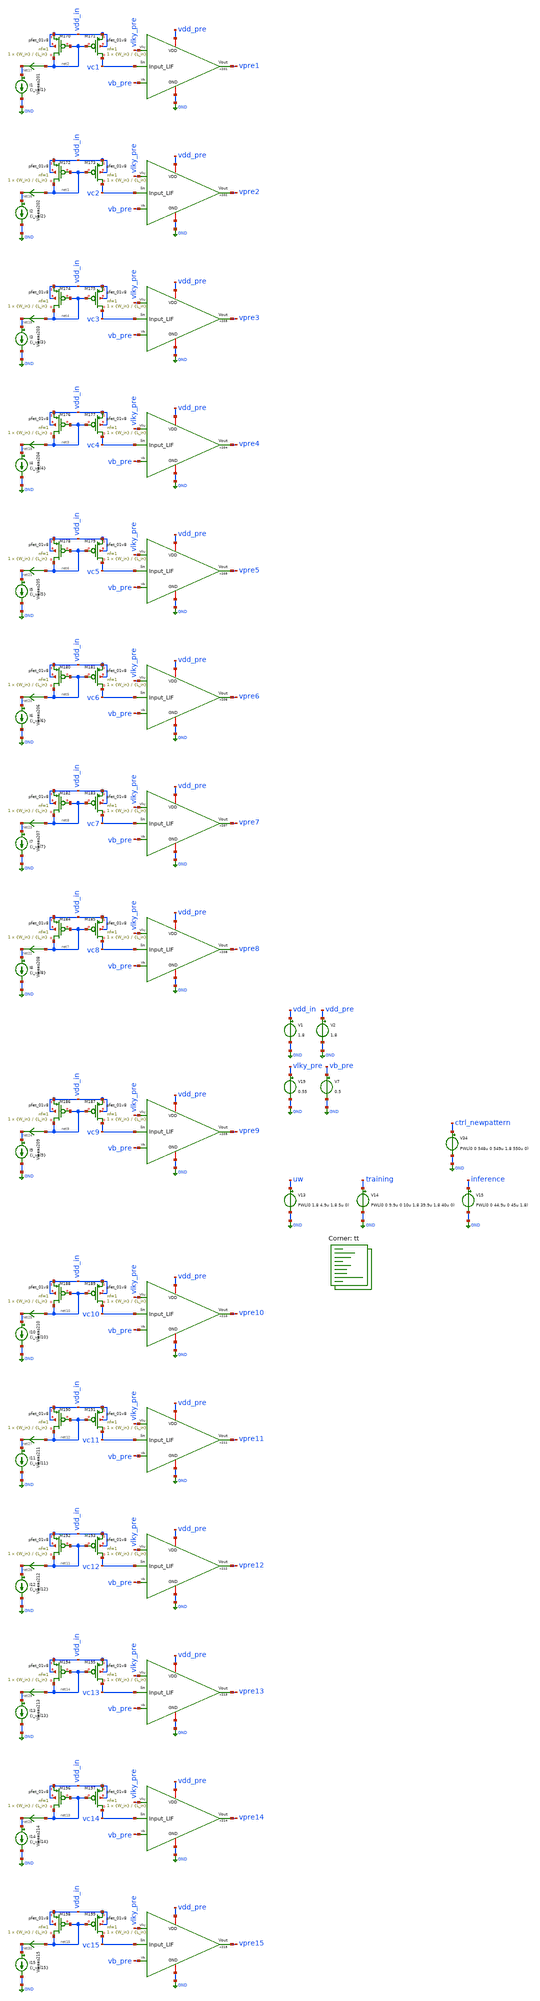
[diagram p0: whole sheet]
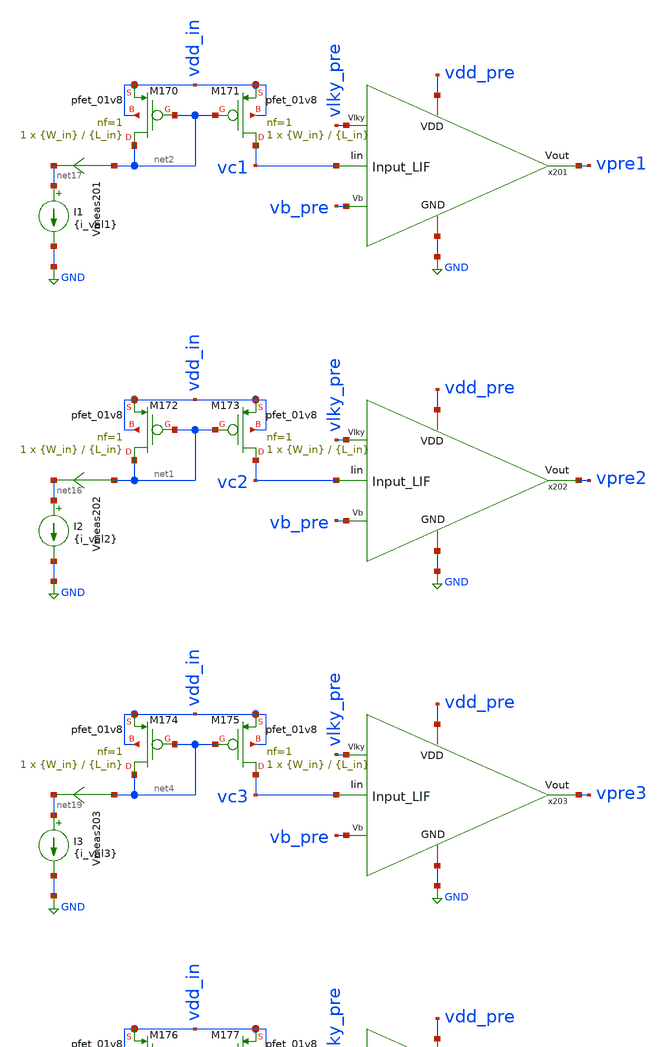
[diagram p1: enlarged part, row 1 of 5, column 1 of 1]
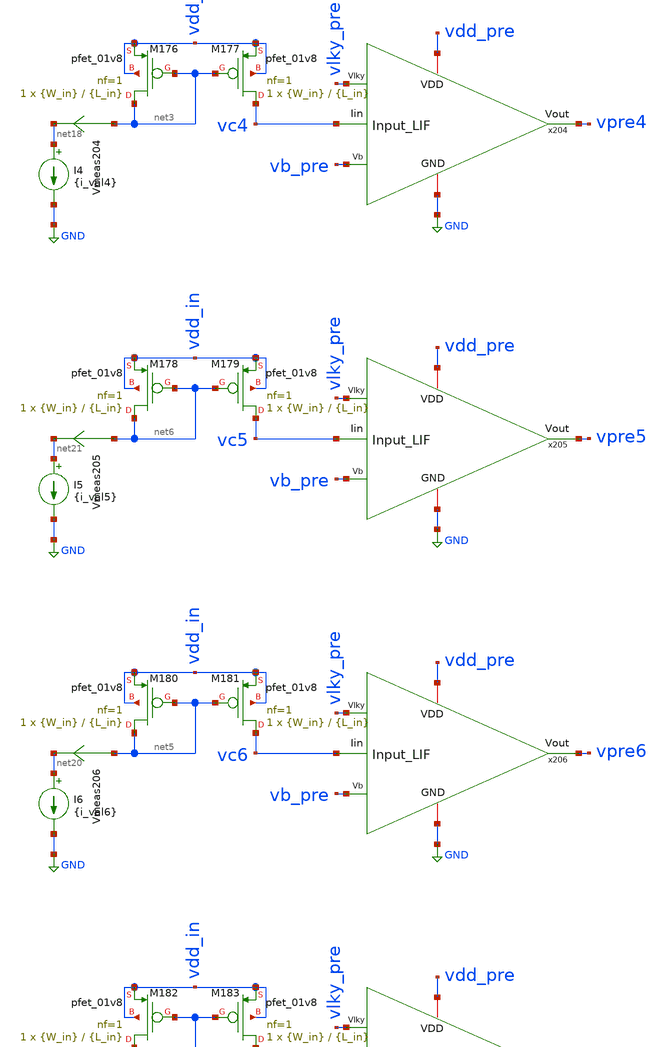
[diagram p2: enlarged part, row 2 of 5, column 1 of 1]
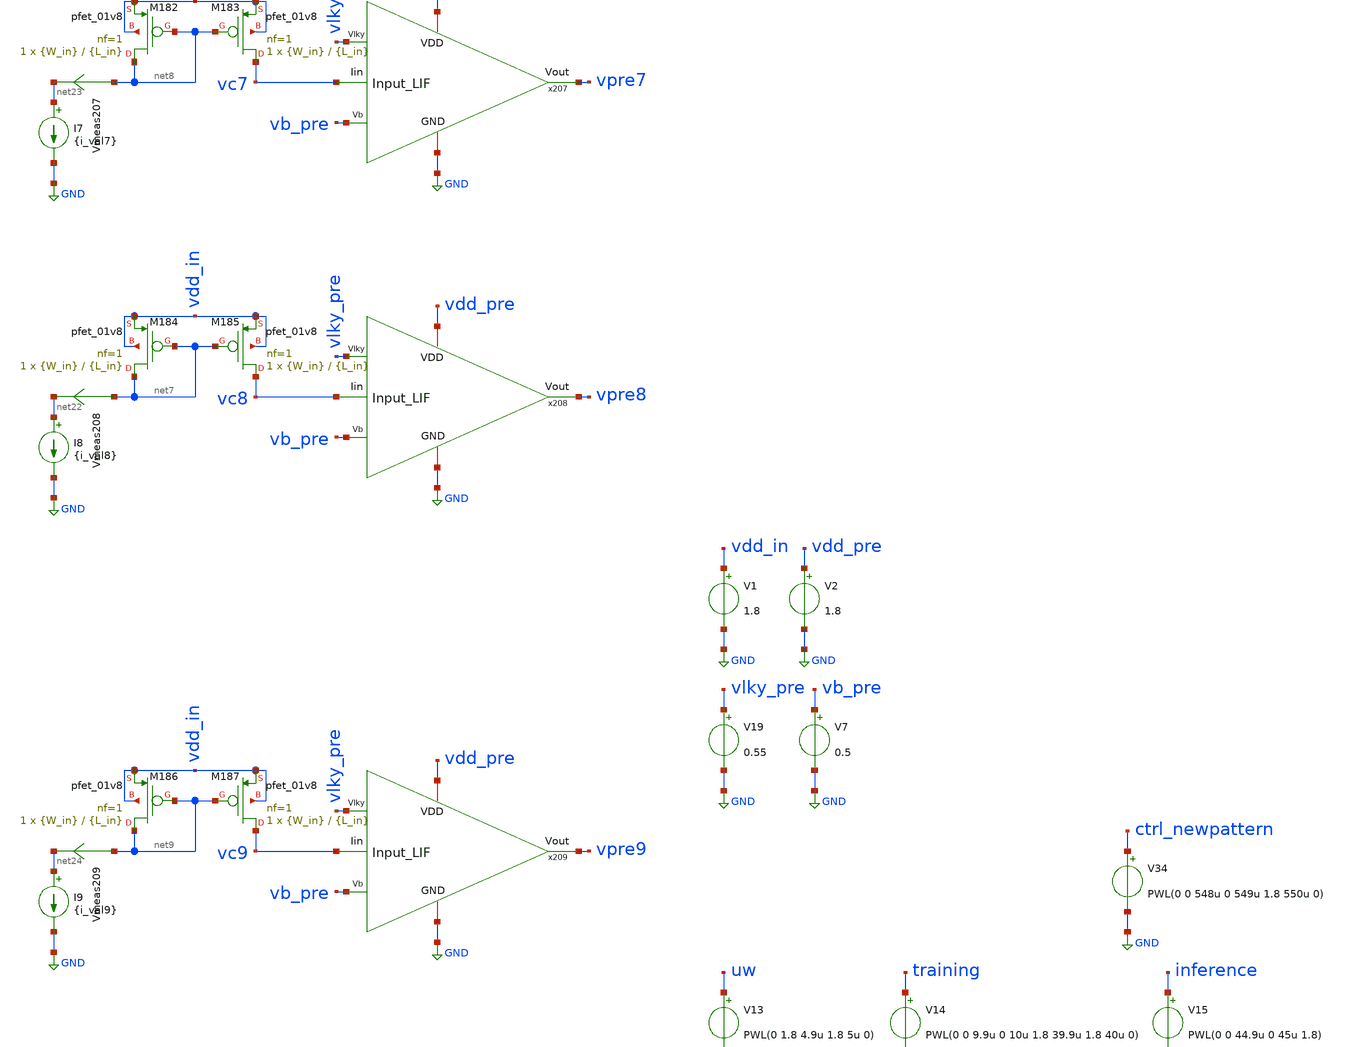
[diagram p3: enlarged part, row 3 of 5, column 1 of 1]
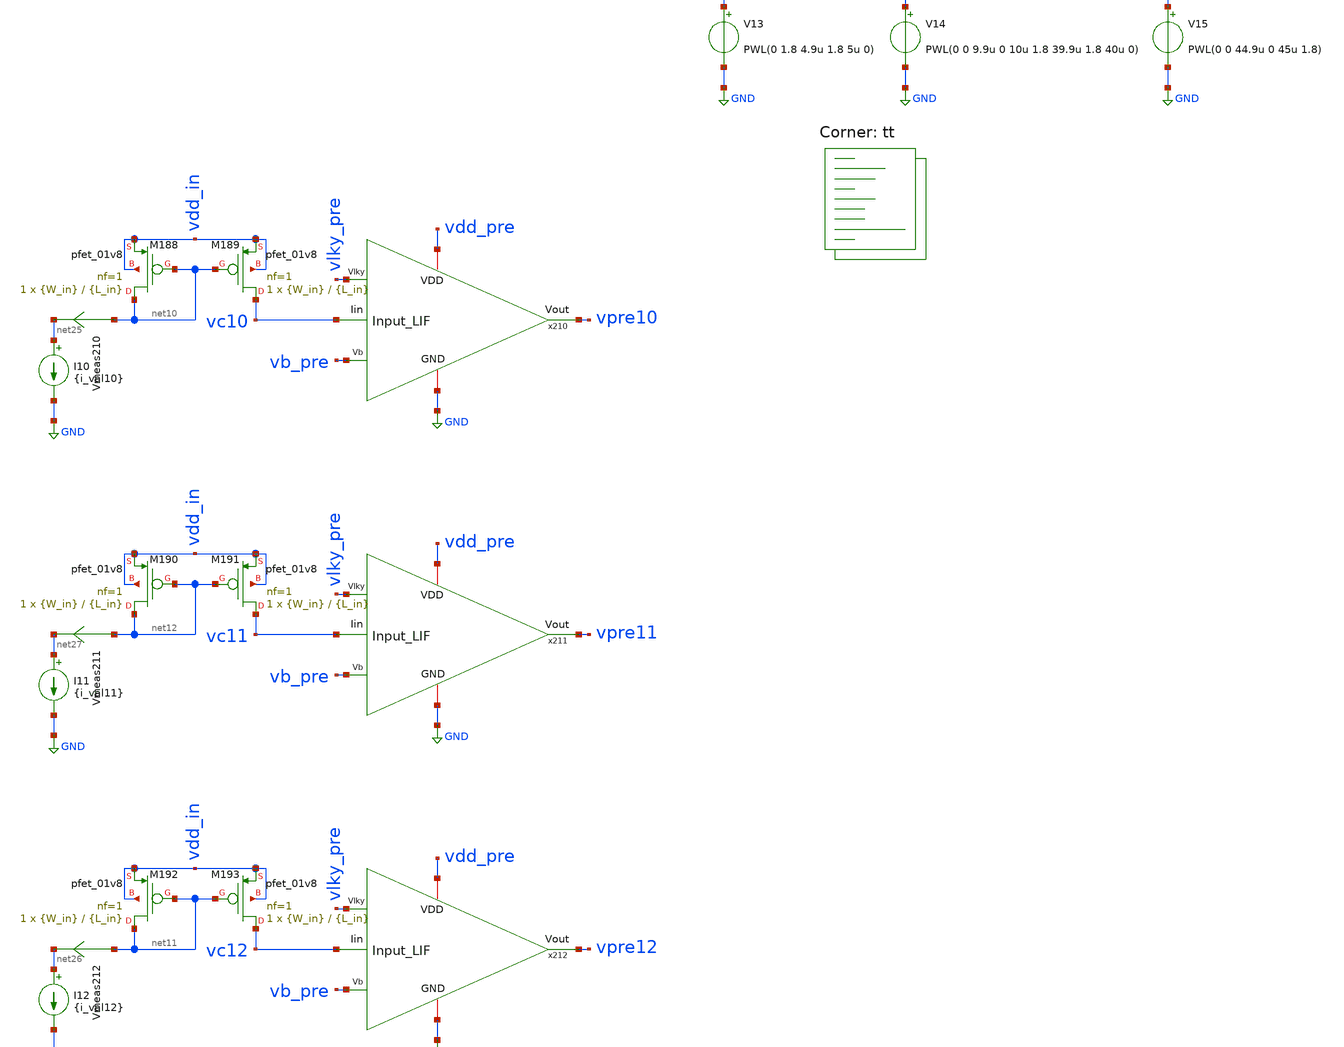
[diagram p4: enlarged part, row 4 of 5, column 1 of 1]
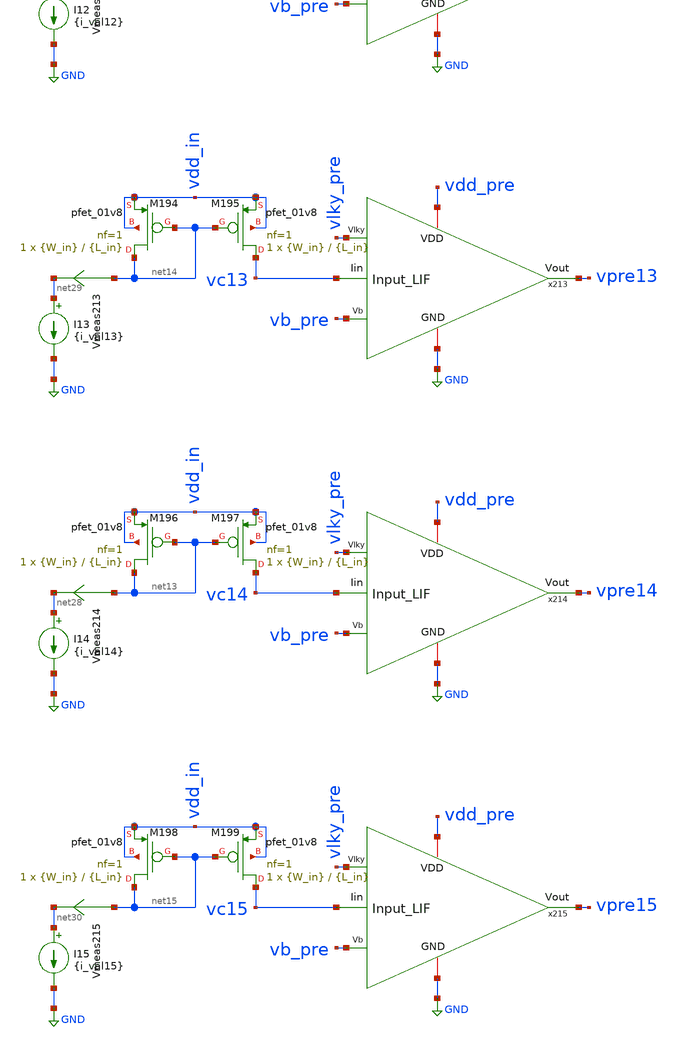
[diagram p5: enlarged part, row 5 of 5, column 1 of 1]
** sch_path: SNN/LIF_15Inputs_N0.sch
**.subckt LIF_15Inputs_N0
V1 vdd_in GND 1.8
V2 vdd_pre GND 1.8
XM173 vc2 net1 vdd_in vdd_in sky130_fd_pr__pfet_01v8 L={L_in} W={W_in} nf=1 ad='int((nf+1)/2) * W/nf * 0.29'
+ as='int((nf+2)/2) * W/nf * 0.29' pd='2*int((nf+1)/2) * (W/nf + 0.29)' ps='2*int((nf+2)/2) * (W/nf + 0.29)'
+ nrd='0.29 / W' nrs='0.29 / W' sa=0 sb=0 sd=0 mult=1 m=1
XM172 net1 net1 vdd_in vdd_in sky130_fd_pr__pfet_01v8 L={L_in} W={W_in} nf=1 ad='int((nf+1)/2) * W/nf * 0.29'
+ as='int((nf+2)/2) * W/nf * 0.29' pd='2*int((nf+1)/2) * (W/nf + 0.29)' ps='2*int((nf+2)/2) * (W/nf + 0.29)'
+ nrd='0.29 / W' nrs='0.29 / W' sa=0 sb=0 sd=0 mult=1 m=1
V13 uw GND PWL(0 1.8 4.9u 1.8 5u 0)
V14 training GND PWL(0 0 9.9u 0 10u 1.8 39.9u 1.8 40u 0)
V15 inference GND PWL(0 0 44.9u 0 45u 1.8)
V7 vb_pre GND 0.5
XM171 vc1 net2 vdd_in vdd_in sky130_fd_pr__pfet_01v8 L={L_in} W={W_in} nf=1 ad='int((nf+1)/2) * W/nf * 0.29'
+ as='int((nf+2)/2) * W/nf * 0.29' pd='2*int((nf+1)/2) * (W/nf + 0.29)' ps='2*int((nf+2)/2) * (W/nf + 0.29)'
+ nrd='0.29 / W' nrs='0.29 / W' sa=0 sb=0 sd=0 mult=1 m=1
XM170 net2 net2 vdd_in vdd_in sky130_fd_pr__pfet_01v8 L={L_in} W={W_in} nf=1 ad='int((nf+1)/2) * W/nf * 0.29'
+ as='int((nf+2)/2) * W/nf * 0.29' pd='2*int((nf+1)/2) * (W/nf + 0.29)' ps='2*int((nf+2)/2) * (W/nf + 0.29)'
+ nrd='0.29 / W' nrs='0.29 / W' sa=0 sb=0 sd=0 mult=1 m=1
V19 vlky_pre GND 0.55
XM177 vc4 net3 vdd_in vdd_in sky130_fd_pr__pfet_01v8 L={L_in} W={W_in} nf=1 ad='int((nf+1)/2) * W/nf * 0.29'
+ as='int((nf+2)/2) * W/nf * 0.29' pd='2*int((nf+1)/2) * (W/nf + 0.29)' ps='2*int((nf+2)/2) * (W/nf + 0.29)'
+ nrd='0.29 / W' nrs='0.29 / W' sa=0 sb=0 sd=0 mult=1 m=1
XM176 net3 net3 vdd_in vdd_in sky130_fd_pr__pfet_01v8 L={L_in} W={W_in} nf=1 ad='int((nf+1)/2) * W/nf * 0.29'
+ as='int((nf+2)/2) * W/nf * 0.29' pd='2*int((nf+1)/2) * (W/nf + 0.29)' ps='2*int((nf+2)/2) * (W/nf + 0.29)'
+ nrd='0.29 / W' nrs='0.29 / W' sa=0 sb=0 sd=0 mult=1 m=1
XM175 vc3 net4 vdd_in vdd_in sky130_fd_pr__pfet_01v8 L={L_in} W={W_in} nf=1 ad='int((nf+1)/2) * W/nf * 0.29'
+ as='int((nf+2)/2) * W/nf * 0.29' pd='2*int((nf+1)/2) * (W/nf + 0.29)' ps='2*int((nf+2)/2) * (W/nf + 0.29)'
+ nrd='0.29 / W' nrs='0.29 / W' sa=0 sb=0 sd=0 mult=1 m=1
XM174 net4 net4 vdd_in vdd_in sky130_fd_pr__pfet_01v8 L={L_in} W={W_in} nf=1 ad='int((nf+1)/2) * W/nf * 0.29'
+ as='int((nf+2)/2) * W/nf * 0.29' pd='2*int((nf+1)/2) * (W/nf + 0.29)' ps='2*int((nf+2)/2) * (W/nf + 0.29)'
+ nrd='0.29 / W' nrs='0.29 / W' sa=0 sb=0 sd=0 mult=1 m=1
XM181 vc6 net5 vdd_in vdd_in sky130_fd_pr__pfet_01v8 L={L_in} W={W_in} nf=1 ad='int((nf+1)/2) * W/nf * 0.29'
+ as='int((nf+2)/2) * W/nf * 0.29' pd='2*int((nf+1)/2) * (W/nf + 0.29)' ps='2*int((nf+2)/2) * (W/nf + 0.29)'
+ nrd='0.29 / W' nrs='0.29 / W' sa=0 sb=0 sd=0 mult=1 m=1
XM180 net5 net5 vdd_in vdd_in sky130_fd_pr__pfet_01v8 L={L_in} W={W_in} nf=1 ad='int((nf+1)/2) * W/nf * 0.29'
+ as='int((nf+2)/2) * W/nf * 0.29' pd='2*int((nf+1)/2) * (W/nf + 0.29)' ps='2*int((nf+2)/2) * (W/nf + 0.29)'
+ nrd='0.29 / W' nrs='0.29 / W' sa=0 sb=0 sd=0 mult=1 m=1
XM179 vc5 net6 vdd_in vdd_in sky130_fd_pr__pfet_01v8 L={L_in} W={W_in} nf=1 ad='int((nf+1)/2) * W/nf * 0.29'
+ as='int((nf+2)/2) * W/nf * 0.29' pd='2*int((nf+1)/2) * (W/nf + 0.29)' ps='2*int((nf+2)/2) * (W/nf + 0.29)'
+ nrd='0.29 / W' nrs='0.29 / W' sa=0 sb=0 sd=0 mult=1 m=1
XM178 net6 net6 vdd_in vdd_in sky130_fd_pr__pfet_01v8 L={L_in} W={W_in} nf=1 ad='int((nf+1)/2) * W/nf * 0.29'
+ as='int((nf+2)/2) * W/nf * 0.29' pd='2*int((nf+1)/2) * (W/nf + 0.29)' ps='2*int((nf+2)/2) * (W/nf + 0.29)'
+ nrd='0.29 / W' nrs='0.29 / W' sa=0 sb=0 sd=0 mult=1 m=1
XM185 vc8 net7 vdd_in vdd_in sky130_fd_pr__pfet_01v8 L={L_in} W={W_in} nf=1 ad='int((nf+1)/2) * W/nf * 0.29'
+ as='int((nf+2)/2) * W/nf * 0.29' pd='2*int((nf+1)/2) * (W/nf + 0.29)' ps='2*int((nf+2)/2) * (W/nf + 0.29)'
+ nrd='0.29 / W' nrs='0.29 / W' sa=0 sb=0 sd=0 mult=1 m=1
XM184 net7 net7 vdd_in vdd_in sky130_fd_pr__pfet_01v8 L={L_in} W={W_in} nf=1 ad='int((nf+1)/2) * W/nf * 0.29'
+ as='int((nf+2)/2) * W/nf * 0.29' pd='2*int((nf+1)/2) * (W/nf + 0.29)' ps='2*int((nf+2)/2) * (W/nf + 0.29)'
+ nrd='0.29 / W' nrs='0.29 / W' sa=0 sb=0 sd=0 mult=1 m=1
XM183 vc7 net8 vdd_in vdd_in sky130_fd_pr__pfet_01v8 L={L_in} W={W_in} nf=1 ad='int((nf+1)/2) * W/nf * 0.29'
+ as='int((nf+2)/2) * W/nf * 0.29' pd='2*int((nf+1)/2) * (W/nf + 0.29)' ps='2*int((nf+2)/2) * (W/nf + 0.29)'
+ nrd='0.29 / W' nrs='0.29 / W' sa=0 sb=0 sd=0 mult=1 m=1
XM182 net8 net8 vdd_in vdd_in sky130_fd_pr__pfet_01v8 L={L_in} W={W_in} nf=1 ad='int((nf+1)/2) * W/nf * 0.29'
+ as='int((nf+2)/2) * W/nf * 0.29' pd='2*int((nf+1)/2) * (W/nf + 0.29)' ps='2*int((nf+2)/2) * (W/nf + 0.29)'
+ nrd='0.29 / W' nrs='0.29 / W' sa=0 sb=0 sd=0 mult=1 m=1
XM187 vc9 net9 vdd_in vdd_in sky130_fd_pr__pfet_01v8 L={L_in} W={W_in} nf=1 ad='int((nf+1)/2) * W/nf * 0.29'
+ as='int((nf+2)/2) * W/nf * 0.29' pd='2*int((nf+1)/2) * (W/nf + 0.29)' ps='2*int((nf+2)/2) * (W/nf + 0.29)'
+ nrd='0.29 / W' nrs='0.29 / W' sa=0 sb=0 sd=0 mult=1 m=1
XM186 net9 net9 vdd_in vdd_in sky130_fd_pr__pfet_01v8 L={L_in} W={W_in} nf=1 ad='int((nf+1)/2) * W/nf * 0.29'
+ as='int((nf+2)/2) * W/nf * 0.29' pd='2*int((nf+1)/2) * (W/nf + 0.29)' ps='2*int((nf+2)/2) * (W/nf + 0.29)'
+ nrd='0.29 / W' nrs='0.29 / W' sa=0 sb=0 sd=0 mult=1 m=1
XM189 vc10 net10 vdd_in vdd_in sky130_fd_pr__pfet_01v8 L={L_in} W={W_in} nf=1 ad='int((nf+1)/2) * W/nf * 0.29'
+ as='int((nf+2)/2) * W/nf * 0.29' pd='2*int((nf+1)/2) * (W/nf + 0.29)' ps='2*int((nf+2)/2) * (W/nf + 0.29)'
+ nrd='0.29 / W' nrs='0.29 / W' sa=0 sb=0 sd=0 mult=1 m=1
XM188 net10 net10 vdd_in vdd_in sky130_fd_pr__pfet_01v8 L={L_in} W={W_in} nf=1 ad='int((nf+1)/2) * W/nf * 0.29'
+ as='int((nf+2)/2) * W/nf * 0.29' pd='2*int((nf+1)/2) * (W/nf + 0.29)' ps='2*int((nf+2)/2) * (W/nf + 0.29)'
+ nrd='0.29 / W' nrs='0.29 / W' sa=0 sb=0 sd=0 mult=1 m=1
XM193 vc12 net11 vdd_in vdd_in sky130_fd_pr__pfet_01v8 L={L_in} W={W_in} nf=1 ad='int((nf+1)/2) * W/nf * 0.29'
+ as='int((nf+2)/2) * W/nf * 0.29' pd='2*int((nf+1)/2) * (W/nf + 0.29)' ps='2*int((nf+2)/2) * (W/nf + 0.29)'
+ nrd='0.29 / W' nrs='0.29 / W' sa=0 sb=0 sd=0 mult=1 m=1
XM192 net11 net11 vdd_in vdd_in sky130_fd_pr__pfet_01v8 L={L_in} W={W_in} nf=1 ad='int((nf+1)/2) * W/nf * 0.29'
+ as='int((nf+2)/2) * W/nf * 0.29' pd='2*int((nf+1)/2) * (W/nf + 0.29)' ps='2*int((nf+2)/2) * (W/nf + 0.29)'
+ nrd='0.29 / W' nrs='0.29 / W' sa=0 sb=0 sd=0 mult=1 m=1
XM191 vc11 net12 vdd_in vdd_in sky130_fd_pr__pfet_01v8 L={L_in} W={W_in} nf=1 ad='int((nf+1)/2) * W/nf * 0.29'
+ as='int((nf+2)/2) * W/nf * 0.29' pd='2*int((nf+1)/2) * (W/nf + 0.29)' ps='2*int((nf+2)/2) * (W/nf + 0.29)'
+ nrd='0.29 / W' nrs='0.29 / W' sa=0 sb=0 sd=0 mult=1 m=1
XM190 net12 net12 vdd_in vdd_in sky130_fd_pr__pfet_01v8 L={L_in} W={W_in} nf=1 ad='int((nf+1)/2) * W/nf * 0.29'
+ as='int((nf+2)/2) * W/nf * 0.29' pd='2*int((nf+1)/2) * (W/nf + 0.29)' ps='2*int((nf+2)/2) * (W/nf + 0.29)'
+ nrd='0.29 / W' nrs='0.29 / W' sa=0 sb=0 sd=0 mult=1 m=1
XM197 vc14 net13 vdd_in vdd_in sky130_fd_pr__pfet_01v8 L={L_in} W={W_in} nf=1 ad='int((nf+1)/2) * W/nf * 0.29'
+ as='int((nf+2)/2) * W/nf * 0.29' pd='2*int((nf+1)/2) * (W/nf + 0.29)' ps='2*int((nf+2)/2) * (W/nf + 0.29)'
+ nrd='0.29 / W' nrs='0.29 / W' sa=0 sb=0 sd=0 mult=1 m=1
XM196 net13 net13 vdd_in vdd_in sky130_fd_pr__pfet_01v8 L={L_in} W={W_in} nf=1 ad='int((nf+1)/2) * W/nf * 0.29'
+ as='int((nf+2)/2) * W/nf * 0.29' pd='2*int((nf+1)/2) * (W/nf + 0.29)' ps='2*int((nf+2)/2) * (W/nf + 0.29)'
+ nrd='0.29 / W' nrs='0.29 / W' sa=0 sb=0 sd=0 mult=1 m=1
XM195 vc13 net14 vdd_in vdd_in sky130_fd_pr__pfet_01v8 L={L_in} W={W_in} nf=1 ad='int((nf+1)/2) * W/nf * 0.29'
+ as='int((nf+2)/2) * W/nf * 0.29' pd='2*int((nf+1)/2) * (W/nf + 0.29)' ps='2*int((nf+2)/2) * (W/nf + 0.29)'
+ nrd='0.29 / W' nrs='0.29 / W' sa=0 sb=0 sd=0 mult=1 m=1
XM194 net14 net14 vdd_in vdd_in sky130_fd_pr__pfet_01v8 L={L_in} W={W_in} nf=1 ad='int((nf+1)/2) * W/nf * 0.29'
+ as='int((nf+2)/2) * W/nf * 0.29' pd='2*int((nf+1)/2) * (W/nf + 0.29)' ps='2*int((nf+2)/2) * (W/nf + 0.29)'
+ nrd='0.29 / W' nrs='0.29 / W' sa=0 sb=0 sd=0 mult=1 m=1
XM199 vc15 net15 vdd_in vdd_in sky130_fd_pr__pfet_01v8 L={L_in} W={W_in} nf=1 ad='int((nf+1)/2) * W/nf * 0.29'
+ as='int((nf+2)/2) * W/nf * 0.29' pd='2*int((nf+1)/2) * (W/nf + 0.29)' ps='2*int((nf+2)/2) * (W/nf + 0.29)'
+ nrd='0.29 / W' nrs='0.29 / W' sa=0 sb=0 sd=0 mult=1 m=1
XM198 net15 net15 vdd_in vdd_in sky130_fd_pr__pfet_01v8 L={L_in} W={W_in} nf=1 ad='int((nf+1)/2) * W/nf * 0.29'
+ as='int((nf+2)/2) * W/nf * 0.29' pd='2*int((nf+1)/2) * (W/nf + 0.29)' ps='2*int((nf+2)/2) * (W/nf + 0.29)'
+ nrd='0.29 / W' nrs='0.29 / W' sa=0 sb=0 sd=0 mult=1 m=1
V34 ctrl_newpattern GND PWL(0 0 548u 0 549u 1.8 550u 0)
x201 vlky_pre vb_pre vdd_pre vpre1 GND vc1 Input_LIF
x202 vlky_pre vb_pre vdd_pre vpre2 GND vc2 Input_LIF
x203 vlky_pre vb_pre vdd_pre vpre3 GND vc3 Input_LIF
x204 vlky_pre vb_pre vdd_pre vpre4 GND vc4 Input_LIF
x205 vlky_pre vb_pre vdd_pre vpre5 GND vc5 Input_LIF
x206 vlky_pre vb_pre vdd_pre vpre6 GND vc6 Input_LIF
x207 vlky_pre vb_pre vdd_pre vpre7 GND vc7 Input_LIF
x208 vlky_pre vb_pre vdd_pre vpre8 GND vc8 Input_LIF
x209 vlky_pre vb_pre vdd_pre vpre9 GND vc9 Input_LIF
x210 vlky_pre vb_pre vdd_pre vpre10 GND vc10 Input_LIF
x211 vlky_pre vb_pre vdd_pre vpre11 GND vc11 Input_LIF
x212 vlky_pre vb_pre vdd_pre vpre12 GND vc12 Input_LIF
x213 vlky_pre vb_pre vdd_pre vpre13 GND vc13 Input_LIF
x214 vlky_pre vb_pre vdd_pre vpre14 GND vc14 Input_LIF
x215 vlky_pre vb_pre vdd_pre vpre15 GND vc15 Input_LIF
I2 net16 GND {i_val2}
Vmeas202 net1 net16 0
.save i(vmeas202)
I1 net17 GND {i_val1}
Vmeas201 net2 net17 0
.save i(vmeas201)
I4 net18 GND {i_val4}
Vmeas204 net3 net18 0
.save i(vmeas204)
I3 net19 GND {i_val3}
Vmeas203 net4 net19 0
.save i(vmeas203)
I6 net20 GND {i_val6}
Vmeas206 net5 net20 0
.save i(vmeas206)
I5 net21 GND {i_val5}
Vmeas205 net6 net21 0
.save i(vmeas205)
I8 net22 GND {i_val8}
Vmeas208 net7 net22 0
.save i(vmeas208)
I7 net23 GND {i_val7}
Vmeas207 net8 net23 0
.save i(vmeas207)
I9 net24 GND {i_val9}
Vmeas209 net9 net24 0
.save i(vmeas209)
I10 net25 GND {i_val10}
Vmeas210 net10 net25 0
.save i(vmeas210)
I12 net26 GND {i_val12}
Vmeas212 net11 net26 0
.save i(vmeas212)
I11 net27 GND {i_val11}
Vmeas211 net12 net27 0
.save i(vmeas211)
I14 net28 GND {i_val14}
Vmeas214 net13 net28 0
.save i(vmeas214)
I13 net29 GND {i_val13}
Vmeas213 net14 net29 0
.save i(vmeas213)
I15 net30 GND {i_val15}
Vmeas215 net15 net30 0
.save i(vmeas215)
**** begin user architecture code
.lib $::SKYWATER_MODELS/sky130.lib.spice tt

** opencircuitdesign pdks install
.inc $::SKYWATER_MODELS/rram_v0.spice



.option set_threads = 16
.option klu
*--Current Injection--*
.param L_in=0.15
.param W_in=1
*--Initial Values--*
.param i_val1=0
.param i_val2=0
.param i_val3=0
.param i_val4=4u
.param i_val5=4u
.param i_val6=4u
.param i_val7=4u
.param i_val8=0
.param i_val9=4u
.param i_val10=4u
.param i_val11=4u
.param i_val12=4u
.param i_val13=0
.param i_val14=0
.param i_val15=0
.control
	save all
	set wr_vecnames
	set wr_singlescale
	*--Clasificación del patrón 0--*
	tran 100n 550u
	write LIF_15Inputs_N0.raw
	wrdata LIF_15inputs_N0.txt v(vpre1) v(vpre2) v(vpre3) v(vpre4) v(vpre5) v(vpre6) v(vpre7) v(vpre8)
+ v(vpre9) v(vpre10) v(vpre11) v(vpre12) v(vpre13) v(vpre14) v(vpre15) v(ctrl_newpattern)
.endc


**** end user architecture code
**.ends

* expanding   symbol:  /home/ricardo/RATT_repos/Proyectos_xschem/SNN/Input_LIF.sym # of pins=6
** sym_path: Final_Design/Input_LIF.sym
** sch_path: Final_Design/Input_LIF.sch
.subckt Input_LIF Vlky Vb VDD Vout GND Iin
*.iopin GND
*.ipin Vb
*.iopin VDD
*.opin Vout
*.ipin Iin
*.ipin Vlky
XM5 net3 Vb GND GND sky130_fd_pr__nfet_01v8 L=0.15 W=5 nf=1 ad='int((nf+1)/2) * W/nf * 0.29' as='int((nf+2)/2) * W/nf * 0.29'
+ pd='2*int((nf+1)/2) * (W/nf + 0.29)' ps='2*int((nf+2)/2) * (W/nf + 0.29)' nrd='0.29 / W' nrs='0.29 / W'
+ sa=0 sb=0 sd=0 mult=1 m=1
XM4 net1 net2 net3 GND sky130_fd_pr__nfet_01v8 L=0.15 W=1.5 nf=1 ad='int((nf+1)/2) * W/nf * 0.29' as='int((nf+2)/2) * W/nf * 0.29'
+ pd='2*int((nf+1)/2) * (W/nf + 0.29)' ps='2*int((nf+2)/2) * (W/nf + 0.29)' nrd='0.29 / W' nrs='0.29 / W'
+ sa=0 sb=0 sd=0 mult=1 m=1
XM3 net1 net2 VDD VDD sky130_fd_pr__pfet_01v8 L=20 W=1 nf=1 ad='int((nf+1)/2) * W/nf * 0.29' as='int((nf+2)/2) * W/nf * 0.29'
+ pd='2*int((nf+1)/2) * (W/nf + 0.29)' ps='2*int((nf+2)/2) * (W/nf + 0.29)' nrd='0.29 / W' nrs='0.29 / W'
+ sa=0 sb=0 sd=0 mult=1 m=1
XC2 net1 GND sky130_fd_pr__cap_mim_m3_1 W=10 L=5 MF=1 m=1
XM2 Iin net1 GND GND sky130_fd_pr__nfet_01v8 L=20 W=1 nf=1 ad='int((nf+1)/2) * W/nf * 0.29' as='int((nf+2)/2) * W/nf * 0.29'
+ pd='2*int((nf+1)/2) * (W/nf + 0.29)' ps='2*int((nf+2)/2) * (W/nf + 0.29)' nrd='0.29 / W' nrs='0.29 / W'
+ sa=0 sb=0 sd=0 mult=1 m=1
XC1 Iin GND sky130_fd_pr__cap_mim_m3_1 W=20 L=20 MF=1 m=1
XM10 net4 Vout GND GND sky130_fd_pr__nfet_01v8 L=0.15 W=1.5 nf=1 ad='int((nf+1)/2) * W/nf * 0.29' as='int((nf+2)/2) * W/nf * 0.29'
+ pd='2*int((nf+1)/2) * (W/nf + 0.29)' ps='2*int((nf+2)/2) * (W/nf + 0.29)' nrd='0.29 / W' nrs='0.29 / W'
+ sa=0 sb=0 sd=0 mult=1 m=1
XM7 net2 Iin net4 GND sky130_fd_pr__nfet_01v8 L=0.15 W=1.5 nf=1 ad='int((nf+1)/2) * W/nf * 0.29' as='int((nf+2)/2) * W/nf * 0.29'
+ pd='2*int((nf+1)/2) * (W/nf + 0.29)' ps='2*int((nf+2)/2) * (W/nf + 0.29)' nrd='0.29 / W' nrs='0.29 / W'
+ sa=0 sb=0 sd=0 mult=1 m=1
XM6 net2 Iin VDD VDD sky130_fd_pr__pfet_01v8 L=0.15 W=1.5 nf=1 ad='int((nf+1)/2) * W/nf * 0.29' as='int((nf+2)/2) * W/nf * 0.29'
+ pd='2*int((nf+1)/2) * (W/nf + 0.29)' ps='2*int((nf+2)/2) * (W/nf + 0.29)' nrd='0.29 / W' nrs='0.29 / W'
+ sa=0 sb=0 sd=0 mult=1 m=1
XM9 Vout net2 net4 GND sky130_fd_pr__nfet_01v8 L=0.15 W=1.5 nf=1 ad='int((nf+1)/2) * W/nf * 0.29' as='int((nf+2)/2) * W/nf * 0.29'
+ pd='2*int((nf+1)/2) * (W/nf + 0.29)' ps='2*int((nf+2)/2) * (W/nf + 0.29)' nrd='0.29 / W' nrs='0.29 / W'
+ sa=0 sb=0 sd=0 mult=1 m=1
XM8 Vout net2 VDD VDD sky130_fd_pr__pfet_01v8 L=0.15 W=5 nf=1 ad='int((nf+1)/2) * W/nf * 0.29' as='int((nf+2)/2) * W/nf * 0.29'
+ pd='2*int((nf+1)/2) * (W/nf + 0.29)' ps='2*int((nf+2)/2) * (W/nf + 0.29)' nrd='0.29 / W' nrs='0.29 / W'
+ sa=0 sb=0 sd=0 mult=1 m=1
XM1 Iin Vlky GND GND sky130_fd_pr__nfet_01v8 L=0.15 W=1.5 nf=1 ad='int((nf+1)/2) * W/nf * 0.29' as='int((nf+2)/2) * W/nf * 0.29'
+ pd='2*int((nf+1)/2) * (W/nf + 0.29)' ps='2*int((nf+2)/2) * (W/nf + 0.29)' nrd='0.29 / W' nrs='0.29 / W'
+ sa=0 sb=0 sd=0 mult=1 m=1
.ends

.GLOBAL GND
.end
